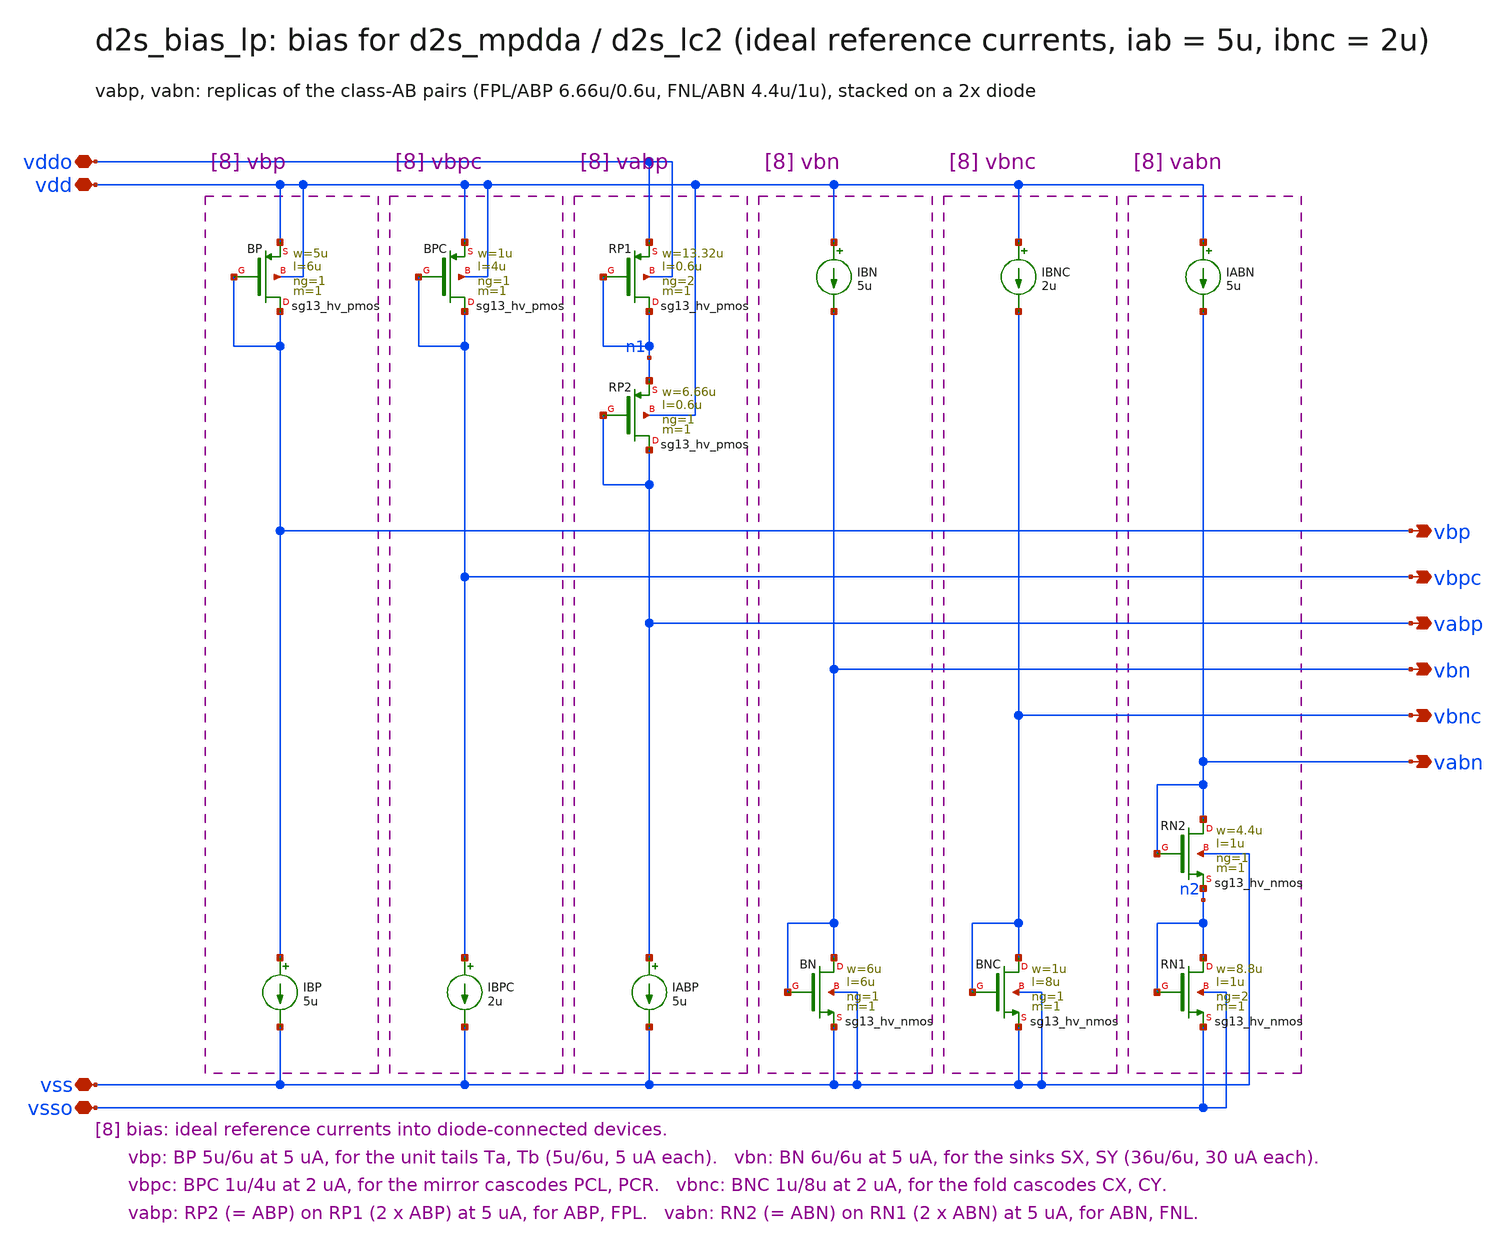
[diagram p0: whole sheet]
** sch_path: sudelbuecher/design_considerations/class_ab_pad_driver/improvements/xschem/d2s_bias_lp.sch
**.subckt d2s_bias_lp vdd vss vddo vsso vbp vbn vbpc vbnc vabp vabn
*.iopin vdd
*.iopin vss
*.iopin vddo
*.iopin vsso
*.opin vbp
*.opin vbn
*.opin vbpc
*.opin vbnc
*.opin vabp
*.opin vabn
XBP vbp vbp vdd vdd sg13_hv_pmos w=5u l=6u ng=1 m=1 mm_ok=1
IBP vbp vss 5u
XBPC vbpc vbpc vdd vdd sg13_hv_pmos w=1u l=4u ng=1 m=1 mm_ok=1
IBPC vbpc vss 2u
XRP1 n1 n1 vddo vddo sg13_hv_pmos w=13.32u l=0.6u ng=2 m=1 mm_ok=1
XRP2 vabp vabp n1 vdd sg13_hv_pmos w=6.66u l=0.6u ng=1 m=1 mm_ok=1
IABP vabp vss 5u
IBN vdd vbn 5u
XBN vbn vbn vss vss sg13_hv_nmos w=6u l=6u ng=1 m=1 mm_ok=1
IBNC vdd vbnc 2u
XBNC vbnc vbnc vss vss sg13_hv_nmos w=1u l=8u ng=1 m=1 mm_ok=1
IABN vdd vabn 5u
XRN2 vabn vabn n2 vss sg13_hv_nmos w=4.4u l=1u ng=1 m=1 mm_ok=1
XRN1 n2 n2 vsso vsso sg13_hv_nmos w=8.8u l=1u ng=2 m=1 mm_ok=1
**.ends
.end
